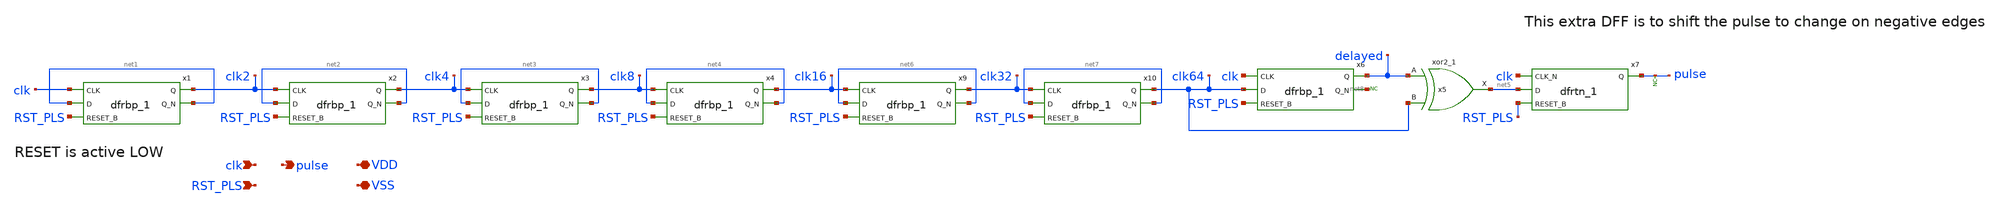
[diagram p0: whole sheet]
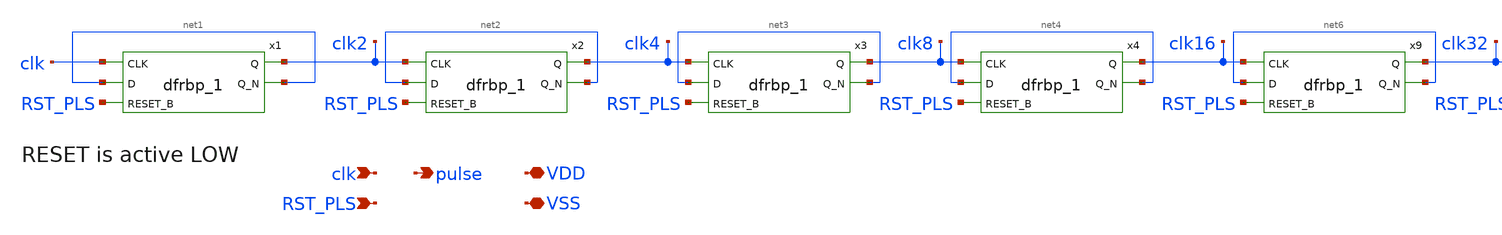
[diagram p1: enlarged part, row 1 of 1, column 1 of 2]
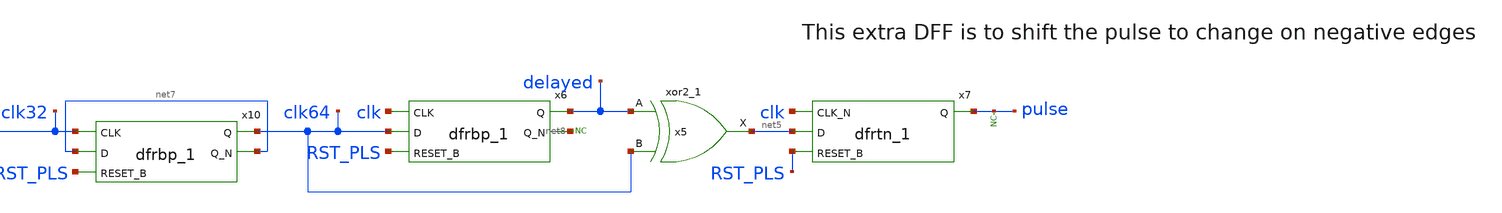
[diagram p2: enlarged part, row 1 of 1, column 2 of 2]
** sch_path: xschem/src/pulse_generator/pulse_generator.sch
**.subckt pulse_generator clk RST_PLS pulse VDD VSS
*.ipin clk
*.ipin RST_PLS
*.opin pulse
*.iopin VDD
*.iopin VSS
x1 clk net1 RST_PLS VSS VSS VDD VDD clk2 net1 sky130_fd_sc_hd__dfrbp_1
x2 clk2 net2 RST_PLS VSS VSS VDD VDD clk4 net2 sky130_fd_sc_hd__dfrbp_1
x3 clk4 net3 RST_PLS VSS VSS VDD VDD clk8 net3 sky130_fd_sc_hd__dfrbp_1
x4 clk8 net4 RST_PLS VSS VSS VDD VDD clk16 net4 sky130_fd_sc_hd__dfrbp_1
x5 delayed clk64 VSS VSS VDD VDD net5 sky130_fd_sc_hd__xor2_1
x6 clk clk64 RST_PLS VSS VSS VDD VDD delayed net8 sky130_fd_sc_hd__dfrbp_1
* noconn #net8
x9 clk16 net6 RST_PLS VSS VSS VDD VDD clk32 net6 sky130_fd_sc_hd__dfrbp_1
x10 clk32 net7 RST_PLS VSS VSS VDD VDD clk64 net7 sky130_fd_sc_hd__dfrbp_1
x7 clk net5 RST_PLS VSS VSS VDD VDD pulse sky130_fd_sc_hd__dfrtn_1
* noconn pulse
**.ends
.end
